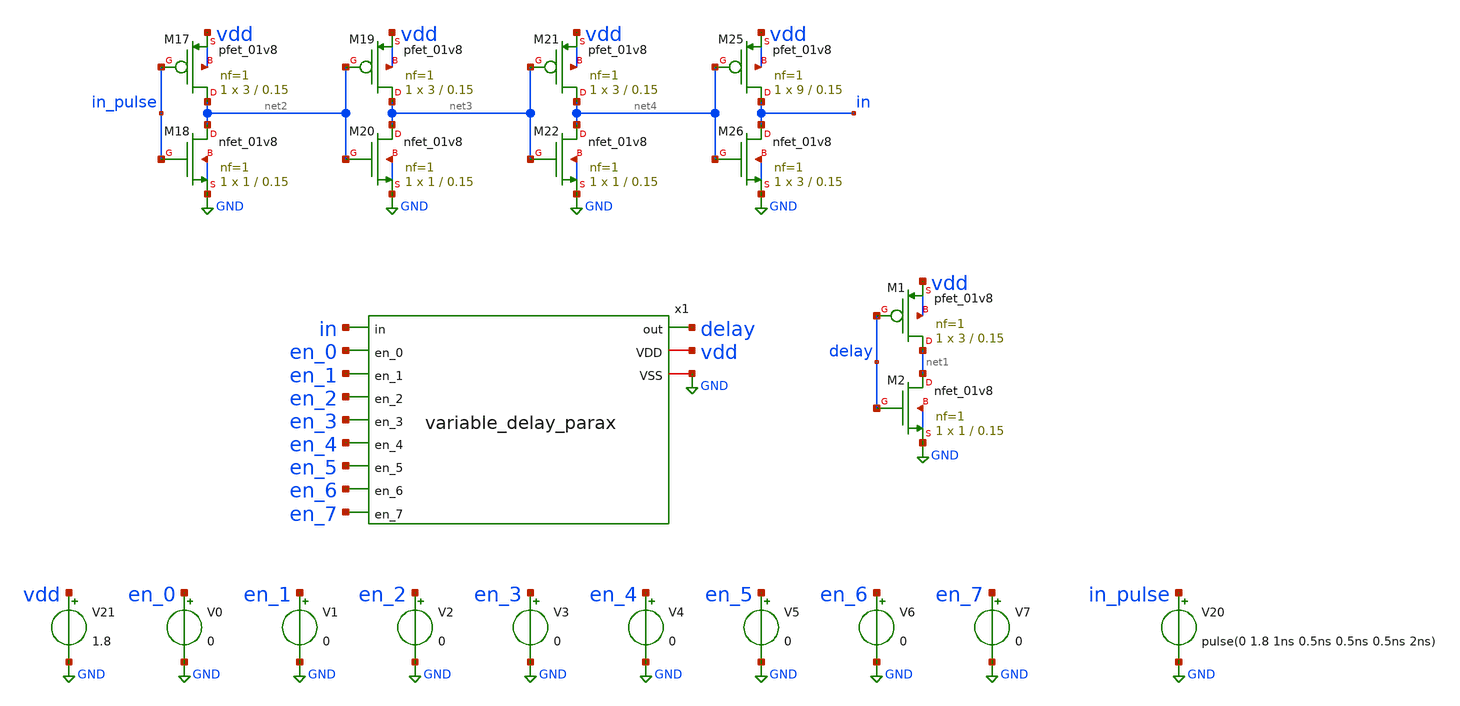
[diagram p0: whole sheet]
** sch_path: xschem/variable_delay_parax_tb.sch
**.subckt variable_delay_parax_tb
x1 in en_0 en_1 en_2 en_3 en_4 en_5 en_6 en_7 delay vdd GND variable_delay_parax
V21 vdd GND 1.8
V20 in_pulse GND pulse(0 1.8 1ns 0.5ns 0.5ns 0.5ns 2ns)
XM1 net1 delay vdd vdd sky130_fd_pr__pfet_01v8 L=0.15 W=3 nf=1 ad='int((nf+1)/2) * W/nf * 0.29' as='int((nf+2)/2) * W/nf * 0.29'
+ pd='2*int((nf+1)/2) * (W/nf + 0.29)' ps='2*int((nf+2)/2) * (W/nf + 0.29)' nrd='0.29 / W' nrs='0.29 / W'
+ sa=0 sb=0 sd=0 mult=1 m=1
XM2 net1 delay GND GND sky130_fd_pr__nfet_01v8 L=0.15 W=1 nf=1 ad='int((nf+1)/2) * W/nf * 0.29' as='int((nf+2)/2) * W/nf * 0.29'
+ pd='2*int((nf+1)/2) * (W/nf + 0.29)' ps='2*int((nf+2)/2) * (W/nf + 0.29)' nrd='0.29 / W' nrs='0.29 / W'
+ sa=0 sb=0 sd=0 mult=1 m=1
V0 en_0 GND 0
V1 en_1 GND 0
V2 en_2 GND 0
V3 en_3 GND 0
V4 en_4 GND 0
V5 en_5 GND 0
V6 en_6 GND 0
V7 en_7 GND 0
XM17 net2 in_pulse vdd vdd sky130_fd_pr__pfet_01v8 L=0.15 W=3 nf=1 ad='int((nf+1)/2) * W/nf * 0.29' as='int((nf+2)/2) * W/nf * 0.29'
+ pd='2*int((nf+1)/2) * (W/nf + 0.29)' ps='2*int((nf+2)/2) * (W/nf + 0.29)' nrd='0.29 / W' nrs='0.29 / W'
+ sa=0 sb=0 sd=0 mult=1 m=1
XM18 net2 in_pulse GND GND sky130_fd_pr__nfet_01v8 L=0.15 W=1 nf=1 ad='int((nf+1)/2) * W/nf * 0.29' as='int((nf+2)/2) * W/nf * 0.29'
+ pd='2*int((nf+1)/2) * (W/nf + 0.29)' ps='2*int((nf+2)/2) * (W/nf + 0.29)' nrd='0.29 / W' nrs='0.29 / W'
+ sa=0 sb=0 sd=0 mult=1 m=1
XM19 net3 net2 vdd vdd sky130_fd_pr__pfet_01v8 L=0.15 W=3 nf=1 ad='int((nf+1)/2) * W/nf * 0.29' as='int((nf+2)/2) * W/nf * 0.29'
+ pd='2*int((nf+1)/2) * (W/nf + 0.29)' ps='2*int((nf+2)/2) * (W/nf + 0.29)' nrd='0.29 / W' nrs='0.29 / W'
+ sa=0 sb=0 sd=0 mult=1 m=1
XM20 net3 net2 GND GND sky130_fd_pr__nfet_01v8 L=0.15 W=1 nf=1 ad='int((nf+1)/2) * W/nf * 0.29' as='int((nf+2)/2) * W/nf * 0.29'
+ pd='2*int((nf+1)/2) * (W/nf + 0.29)' ps='2*int((nf+2)/2) * (W/nf + 0.29)' nrd='0.29 / W' nrs='0.29 / W'
+ sa=0 sb=0 sd=0 mult=1 m=1
XM21 net4 net3 vdd vdd sky130_fd_pr__pfet_01v8 L=0.15 W=3 nf=1 ad='int((nf+1)/2) * W/nf * 0.29' as='int((nf+2)/2) * W/nf * 0.29'
+ pd='2*int((nf+1)/2) * (W/nf + 0.29)' ps='2*int((nf+2)/2) * (W/nf + 0.29)' nrd='0.29 / W' nrs='0.29 / W'
+ sa=0 sb=0 sd=0 mult=1 m=1
XM22 net4 net3 GND GND sky130_fd_pr__nfet_01v8 L=0.15 W=1 nf=1 ad='int((nf+1)/2) * W/nf * 0.29' as='int((nf+2)/2) * W/nf * 0.29'
+ pd='2*int((nf+1)/2) * (W/nf + 0.29)' ps='2*int((nf+2)/2) * (W/nf + 0.29)' nrd='0.29 / W' nrs='0.29 / W'
+ sa=0 sb=0 sd=0 mult=1 m=1
XM25 in net4 vdd vdd sky130_fd_pr__pfet_01v8 L=0.15 W=9 nf=1 ad='int((nf+1)/2) * W/nf * 0.29' as='int((nf+2)/2) * W/nf * 0.29'
+ pd='2*int((nf+1)/2) * (W/nf + 0.29)' ps='2*int((nf+2)/2) * (W/nf + 0.29)' nrd='0.29 / W' nrs='0.29 / W'
+ sa=0 sb=0 sd=0 mult=1 m=1
XM26 in net4 GND GND sky130_fd_pr__nfet_01v8 L=0.15 W=3 nf=1 ad='int((nf+1)/2) * W/nf * 0.29' as='int((nf+2)/2) * W/nf * 0.29'
+ pd='2*int((nf+1)/2) * (W/nf + 0.29)' ps='2*int((nf+2)/2) * (W/nf + 0.29)' nrd='0.29 / W' nrs='0.29 / W'
+ sa=0 sb=0 sd=0 mult=1 m=1
**** begin user architecture code

** opencircuitdesign pdks install
.lib $::SKYWATER_MODELS/sky130.lib.spice tt





.control
foreach i 0 1 2 3 4 5 6 7
* Set all sources to 0 initially
alter V0 0
alter V1 0
alter V2 0
alter V3 0
alter V4 0
alter V5 0
alter V6 0
alter V7 0

* Set the current source to 1.8V
alter V$i 1.8

* Run transient analysis
tran 0.0001n 5n

* Save results for this step
save v(in) v(delay)
set wr_vecnames
wrdata variable_delay_tb_$i v(in) v(delay)

end
.endc


**** end user architecture code
**.ends

* expanding   symbol:  variable_delay_parax.sym # of pins=12
** sym_path: xschem/variable_delay.sym
.include [file normalize ../mag/variable_delay.sim.spice]
.GLOBAL GND
.end
